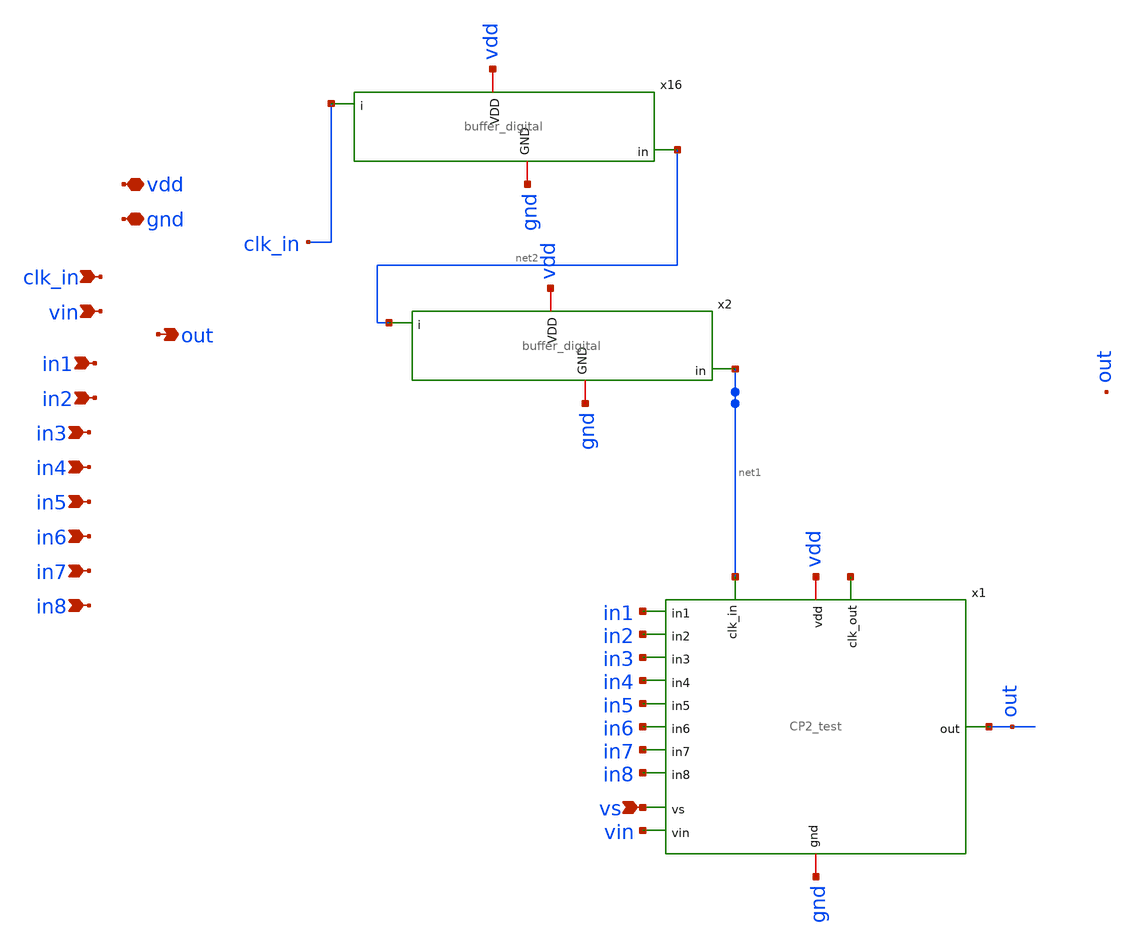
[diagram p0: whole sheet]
** sch_path: xschem/cp2_buffer_xschem.sch
**.subckt cp2_buffer_xschem clk_in gnd vdd out vin in1 in2 in3 in4 in5 in6 in7 in8 vs
*.ipin clk_in
*.iopin gnd
*.iopin vdd
*.opin out
*.ipin vin
*.ipin in1
*.ipin in2
*.ipin in3
*.ipin in4
*.ipin in5
*.ipin in6
*.ipin in7
*.ipin in8
*.ipin vs
x16 gnd vdd clk_in net2 buffer_digital
x1 gnd vs net1 vin out in1 in2 in3 in4 in5 in6 in7 in8 vdd net3 CP2_test
x2 gnd vdd net2 net1 buffer_digital
**.ends
.end
